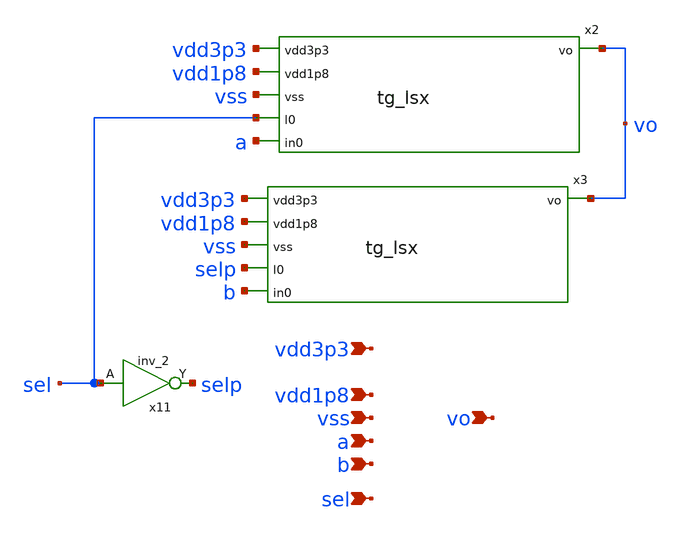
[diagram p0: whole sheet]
** sch_path: schematic/EF_amux21x.sch
**.subckt EF_amux21x vdd1p8 vss a b vdd3p3 sel vo
*.ipin vdd1p8
*.ipin vss
*.ipin a
*.ipin b
*.ipin vdd3p3
*.ipin sel
*.ipin vo
x2 vdd3p3 vdd1p8 vss sel vo a tg_lsx
x3 vdd3p3 vdd1p8 vss selp vo b tg_lsx
x11 sel vss vss vdd3p3 vdd3p3 selp sky130_fd_sc_hvl__inv_2
**.ends
.end
